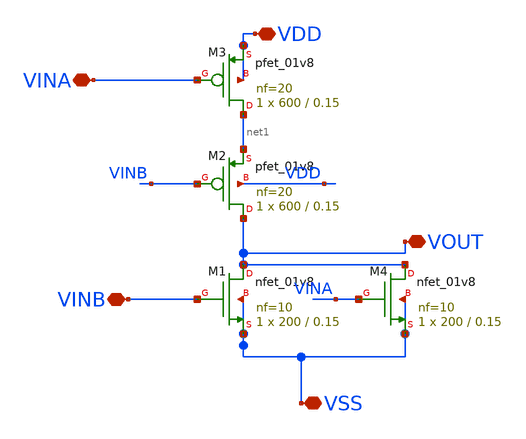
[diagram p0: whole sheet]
** sch_path: xschem/DC_DC_Converter_xschem/OTHERS/DC_DC_Converter_6/Delay_block_revised/NOR.sch
**.subckt NOR VDD VSS VINB VINA VOUT
*.iopin VDD
*.iopin VSS
*.iopin VINB
*.iopin VINA
*.iopin VOUT
XM1 VOUT VINB VSS VSS sky130_fd_pr__nfet_01v8 L=0.15 W=200 nf=10 ad='int((nf+1)/2) * W/nf * 0.29' as='int((nf+2)/2) * W/nf * 0.29'
+ pd='2*int((nf+1)/2) * (W/nf + 0.29)' ps='2*int((nf+2)/2) * (W/nf + 0.29)' nrd='0.29 / W' nrs='0.29 / W'
+ sa=0 sb=0 sd=0 mult=1 m=1
XM2 VOUT VINB net1 VDD sky130_fd_pr__pfet_01v8 L=0.15 W=600 nf=20 ad='int((nf+1)/2) * W/nf * 0.29' as='int((nf+2)/2) * W/nf * 0.29'
+ pd='2*int((nf+1)/2) * (W/nf + 0.29)' ps='2*int((nf+2)/2) * (W/nf + 0.29)' nrd='0.29 / W' nrs='0.29 / W'
+ sa=0 sb=0 sd=0 mult=1 m=1
XM3 net1 VINA VDD VDD sky130_fd_pr__pfet_01v8 L=0.15 W=600 nf=20 ad='int((nf+1)/2) * W/nf * 0.29' as='int((nf+2)/2) * W/nf * 0.29'
+ pd='2*int((nf+1)/2) * (W/nf + 0.29)' ps='2*int((nf+2)/2) * (W/nf + 0.29)' nrd='0.29 / W' nrs='0.29 / W'
+ sa=0 sb=0 sd=0 mult=1 m=1
XM4 VOUT VINA VSS VSS sky130_fd_pr__nfet_01v8 L=0.15 W=200 nf=10 ad='int((nf+1)/2) * W/nf * 0.29' as='int((nf+2)/2) * W/nf * 0.29'
+ pd='2*int((nf+1)/2) * (W/nf + 0.29)' ps='2*int((nf+2)/2) * (W/nf + 0.29)' nrd='0.29 / W' nrs='0.29 / W'
+ sa=0 sb=0 sd=0 mult=1 m=1
**.ends
.end
